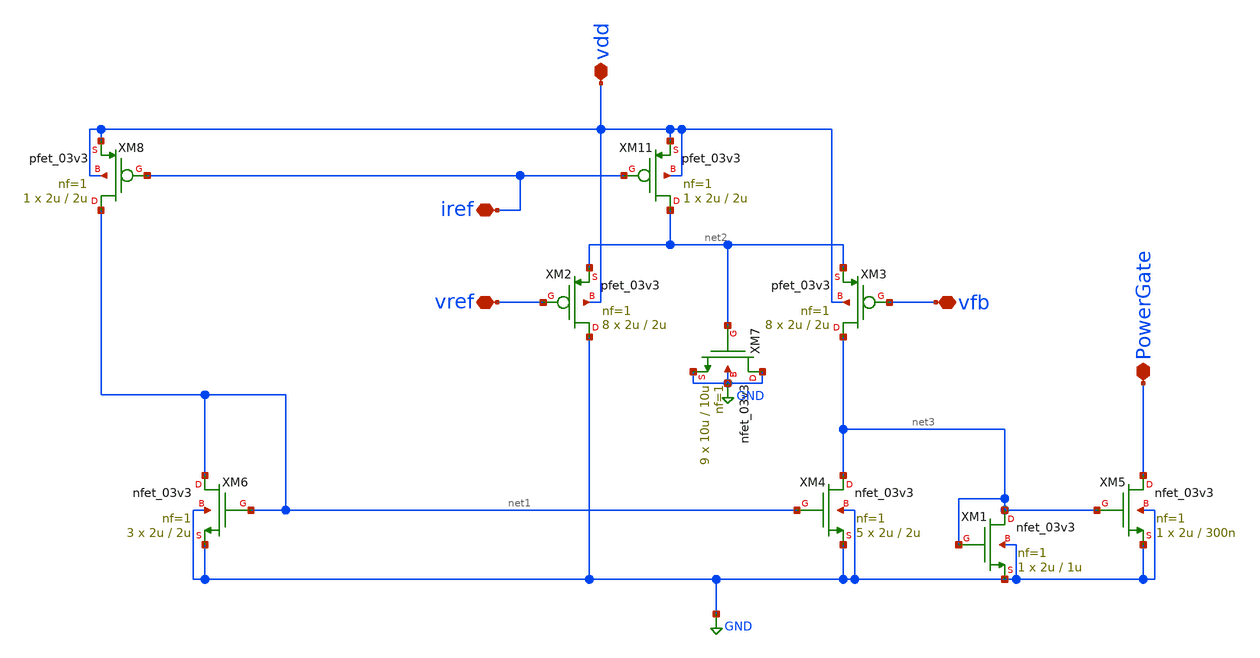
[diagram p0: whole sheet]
** sch_path: Voltage_Reference/LDO/UndervoltageProtection.sch
**.subckt UndervoltageProtection PowerGate vfb vref iref vdd
*.iopin PowerGate
*.iopin vfb
*.iopin vref
*.iopin iref
*.iopin vdd
XM2 GND vref net2 vdd pfet_03v3 L=2u W=2u nf=1 ad='int((nf+1)/2) * W/nf * 0.18u' as='int((nf+2)/2) * W/nf * 0.18u'
+ pd='2*int((nf+1)/2) * (W/nf + 0.18u)' ps='2*int((nf+2)/2) * (W/nf + 0.18u)' nrd='0.18u / W' nrs='0.18u / W'
+ sa=0 sb=0 sd=0 m=8
XM3 net3 vfb net2 vdd pfet_03v3 L=2u W=2u nf=1 ad='int((nf+1)/2) * W/nf * 0.18u' as='int((nf+2)/2) * W/nf * 0.18u'
+ pd='2*int((nf+1)/2) * (W/nf + 0.18u)' ps='2*int((nf+2)/2) * (W/nf + 0.18u)' nrd='0.18u / W' nrs='0.18u / W'
+ sa=0 sb=0 sd=0 m=8
XM4 net3 net1 GND GND nfet_03v3 L=2u W=2u nf=1 ad='int((nf+1)/2) * W/nf * 0.18u' as='int((nf+2)/2) * W/nf * 0.18u'
+ pd='2*int((nf+1)/2) * (W/nf + 0.18u)' ps='2*int((nf+2)/2) * (W/nf + 0.18u)' nrd='0.18u / W' nrs='0.18u / W'
+ sa=0 sb=0 sd=0 m=5
XM5 PowerGate net3 GND GND nfet_03v3 L=300n W=2u nf=1 ad='int((nf+1)/2) * W/nf * 0.18u' as='int((nf+2)/2) * W/nf * 0.18u'
+ pd='2*int((nf+1)/2) * (W/nf + 0.18u)' ps='2*int((nf+2)/2) * (W/nf + 0.18u)' nrd='0.18u / W' nrs='0.18u / W'
+ sa=0 sb=0 sd=0 m=1
XM6 net1 net1 GND GND nfet_03v3 L=2u W=2u nf=1 ad='int((nf+1)/2) * W/nf * 0.18u' as='int((nf+2)/2) * W/nf * 0.18u'
+ pd='2*int((nf+1)/2) * (W/nf + 0.18u)' ps='2*int((nf+2)/2) * (W/nf + 0.18u)' nrd='0.18u / W' nrs='0.18u / W'
+ sa=0 sb=0 sd=0 m=3
XM7 GND net2 GND GND nfet_03v3 L=10u W=10u nf=1 ad='int((nf+1)/2) * W/nf * 0.18u' as='int((nf+2)/2) * W/nf * 0.18u'
+ pd='2*int((nf+1)/2) * (W/nf + 0.18u)' ps='2*int((nf+2)/2) * (W/nf + 0.18u)' nrd='0.18u / W' nrs='0.18u / W'
+ sa=0 sb=0 sd=0 m=9
XM11 net2 iref vdd vdd pfet_03v3 L=2u W=2u nf=1 ad='int((nf+1)/2) * W/nf * 0.18u' as='int((nf+2)/2) * W/nf * 0.18u'
+ pd='2*int((nf+1)/2) * (W/nf + 0.18u)' ps='2*int((nf+2)/2) * (W/nf + 0.18u)' nrd='0.18u / W' nrs='0.18u / W'
+ sa=0 sb=0 sd=0 m=1
XM8 net1 iref vdd vdd pfet_03v3 L=2u W=2u nf=1 ad='int((nf+1)/2) * W/nf * 0.18u' as='int((nf+2)/2) * W/nf * 0.18u'
+ pd='2*int((nf+1)/2) * (W/nf + 0.18u)' ps='2*int((nf+2)/2) * (W/nf + 0.18u)' nrd='0.18u / W' nrs='0.18u / W'
+ sa=0 sb=0 sd=0 m=1
XM1 net3 net3 GND GND nfet_03v3 L=1u W=2u nf=1 ad='int((nf+1)/2) * W/nf * 0.18u' as='int((nf+2)/2) * W/nf * 0.18u'
+ pd='2*int((nf+1)/2) * (W/nf + 0.18u)' ps='2*int((nf+2)/2) * (W/nf + 0.18u)' nrd='0.18u / W' nrs='0.18u / W'
+ sa=0 sb=0 sd=0 m=1
**.ends
.GLOBAL GND
.end
